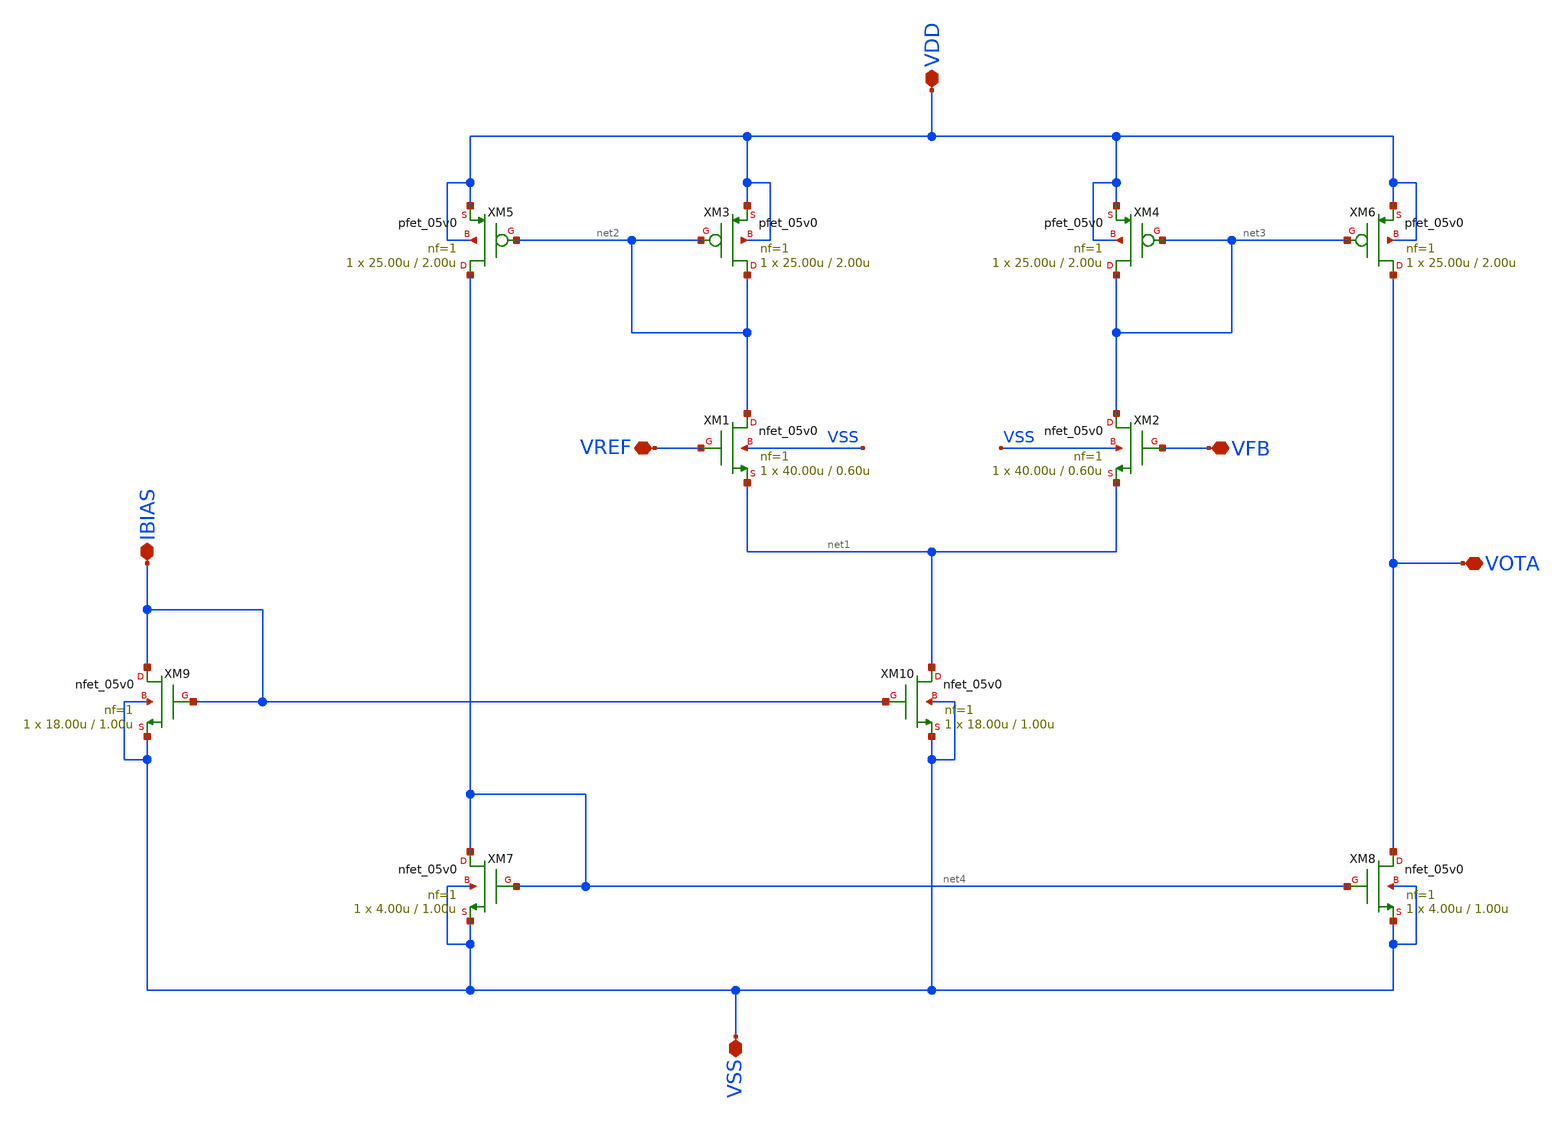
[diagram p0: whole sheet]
** sch_path: designs/libs/core_ldo/ldo/ldo_OTA/OTA.sch
**.subckt OTA VDD VSS VOTA VREF IBIAS VFB
*.iopin VDD
*.iopin VSS
*.iopin VOTA
*.iopin VREF
*.iopin IBIAS
*.iopin VFB
XM3 net2 net2 VDD VDD pfet_05v0 L=2.00u W=25.00u nf=1 ad='int((nf+1)/2) * W/nf * 0.18u' as='int((nf+2)/2) * W/nf * 0.18u'
+ pd='2*int((nf+1)/2) * (W/nf + 0.18u)' ps='2*int((nf+2)/2) * (W/nf + 0.18u)' nrd='0.18u / W' nrs='0.18u / W'
+ sa=0 sb=0 sd=0 m=1
XM4 net3 net3 VDD VDD pfet_05v0 L=2.00u W=25.00u nf=1 ad='int((nf+1)/2) * W/nf * 0.18u' as='int((nf+2)/2) * W/nf * 0.18u'
+ pd='2*int((nf+1)/2) * (W/nf + 0.18u)' ps='2*int((nf+2)/2) * (W/nf + 0.18u)' nrd='0.18u / W' nrs='0.18u / W'
+ sa=0 sb=0 sd=0 m=1
XM5 net4 net2 VDD VDD pfet_05v0 L=2.00u W=25.00u nf=1 ad='int((nf+1)/2) * W/nf * 0.18u' as='int((nf+2)/2) * W/nf * 0.18u'
+ pd='2*int((nf+1)/2) * (W/nf + 0.18u)' ps='2*int((nf+2)/2) * (W/nf + 0.18u)' nrd='0.18u / W' nrs='0.18u / W'
+ sa=0 sb=0 sd=0 m=1
XM6 VOTA net3 VDD VDD pfet_05v0 L=2.00u W=25.00u nf=1 ad='int((nf+1)/2) * W/nf * 0.18u' as='int((nf+2)/2) * W/nf * 0.18u'
+ pd='2*int((nf+1)/2) * (W/nf + 0.18u)' ps='2*int((nf+2)/2) * (W/nf + 0.18u)' nrd='0.18u / W' nrs='0.18u / W'
+ sa=0 sb=0 sd=0 m=1
XM9 IBIAS IBIAS VSS VSS nfet_05v0 L=1.00u W=18.00u nf=1 ad='int((nf+1)/2) * W/nf * 0.18u' as='int((nf+2)/2) * W/nf * 0.18u'
+ pd='2*int((nf+1)/2) * (W/nf + 0.18u)' ps='2*int((nf+2)/2) * (W/nf + 0.18u)' nrd='0.18u / W' nrs='0.18u / W'
+ sa=0 sb=0 sd=0 m=1
XM10 net1 IBIAS VSS VSS nfet_05v0 L=1.00u W=18.00u nf=1 ad='int((nf+1)/2) * W/nf * 0.18u' as='int((nf+2)/2) * W/nf * 0.18u'
+ pd='2*int((nf+1)/2) * (W/nf + 0.18u)' ps='2*int((nf+2)/2) * (W/nf + 0.18u)' nrd='0.18u / W' nrs='0.18u / W'
+ sa=0 sb=0 sd=0 m=1
XM7 net4 net4 VSS VSS nfet_05v0 L=1.00u W=4.00u nf=1 ad='int((nf+1)/2) * W/nf * 0.18u' as='int((nf+2)/2) * W/nf * 0.18u'
+ pd='2*int((nf+1)/2) * (W/nf + 0.18u)' ps='2*int((nf+2)/2) * (W/nf + 0.18u)' nrd='0.18u / W' nrs='0.18u / W'
+ sa=0 sb=0 sd=0 m=1
XM8 VOTA net4 VSS VSS nfet_05v0 L=1.00u W=4.00u nf=1 ad='int((nf+1)/2) * W/nf * 0.18u' as='int((nf+2)/2) * W/nf * 0.18u'
+ pd='2*int((nf+1)/2) * (W/nf + 0.18u)' ps='2*int((nf+2)/2) * (W/nf + 0.18u)' nrd='0.18u / W' nrs='0.18u / W'
+ sa=0 sb=0 sd=0 m=1
XM1 net2 VREF net1 VSS nfet_05v0 L=0.60u W=40.00u nf=1 ad='int((nf+1)/2) * W/nf * 0.18u' as='int((nf+2)/2) * W/nf * 0.18u'
+ pd='2*int((nf+1)/2) * (W/nf + 0.18u)' ps='2*int((nf+2)/2) * (W/nf + 0.18u)' nrd='0.18u / W' nrs='0.18u / W'
+ sa=0 sb=0 sd=0 m=1
XM2 net3 VFB net1 VSS nfet_05v0 L=0.60u W=40.00u nf=1 ad='int((nf+1)/2) * W/nf * 0.18u' as='int((nf+2)/2) * W/nf * 0.18u'
+ pd='2*int((nf+1)/2) * (W/nf + 0.18u)' ps='2*int((nf+2)/2) * (W/nf + 0.18u)' nrd='0.18u / W' nrs='0.18u / W'
+ sa=0 sb=0 sd=0 m=1
**.ends
.end
